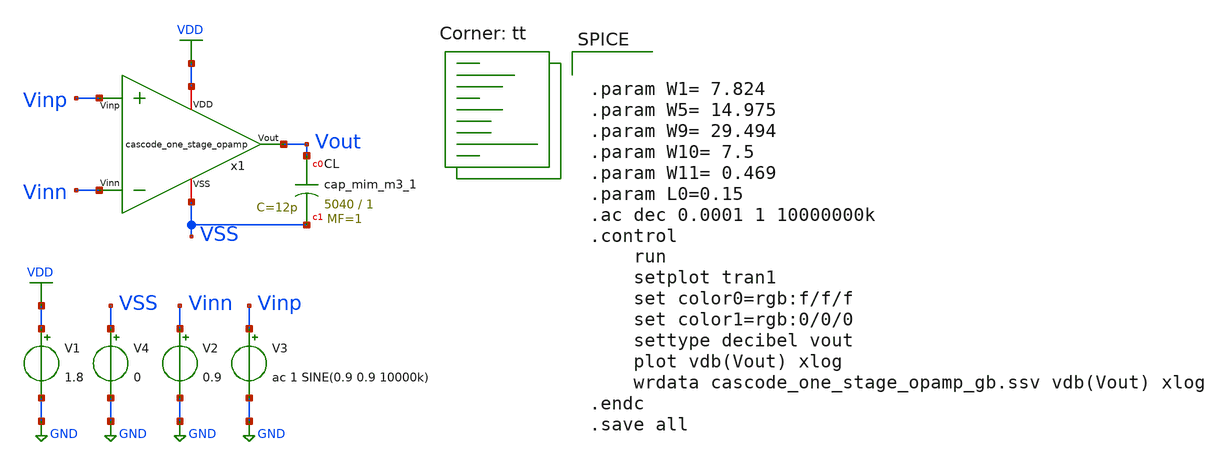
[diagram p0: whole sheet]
** sch_path: opamp_design/cascode_one_stage_opamp/cascode_one_stage_opamp_gb.sch
**.subckt cascode_one_stage_opamp_gb
V1 VDD GND 1.8
V2 Vinn GND 0.9
V3 Vinp GND ac 1 SINE(0.9 0.9 10000k)
V4 VSS GND 0
XCL Vout VSS sky130_fd_pr__cap_mim_m3_1 W=5040 L=1 MF=1 m=1
x1 VDD Vout Vinp Vinn VSS cascode_one_stage_opamp
**** begin user architecture code


.param W1= 7.824
.param W5= 14.975
.param W9= 29.494
.param W10= 7.5
.param W11= 0.469
.param L0=0.15
.ac dec 0.0001 1 10000000k
.control
	run
	setplot tran1
	set color0=rgb:f/f/f
	set color1=rgb:0/0/0
	settype decibel vout
	plot vdb(Vout) xlog
	wrdata cascode_one_stage_opamp_gb.ssv vdb(Vout) xlog
.endc
.save all


.lib $::SKYWATER_MODELS/sky130.lib.spice tt
**** end user architecture code
**.ends

* expanding   symbol:
*+  /home/ricardo/RATT_repos/Proyectos_xschem/opamp_design/cascode_one_stage_opamp/cascode_one_stage_opamp.sym # of pins=5
** sym_path: opamp_design/cascode_one_stage_opamp/cascode_one_stage_opamp.sym
** sch_path: opamp_design/cascode_one_stage_opamp/cascode_one_stage_opamp.sch
.subckt cascode_one_stage_opamp VDD Vout Vinp Vinn VSS
*.ipin Vinp
*.ipin Vinn
*.opin Vout
*.iopin VDD
*.iopin VSS
XM1 net6 Vinp net1 VSS sky130_fd_pr__nfet_01v8 L={L0} W={W1} nf=1 ad='int((nf+1)/2) * W/nf * 0.29' as='int((nf+2)/2) * W/nf * 0.29'
+ pd='2*int((nf+1)/2) * (W/nf + 0.29)' ps='2*int((nf+2)/2) * (W/nf + 0.29)' nrd='0.29 / W' nrs='0.29 / W'
+ sa=0 sb=0 sd=0 mult=1 m=1
XM2 net7 Vinn net1 VSS sky130_fd_pr__nfet_01v8 L={L0} W={W1} nf=1 ad='int((nf+1)/2) * W/nf * 0.29' as='int((nf+2)/2) * W/nf * 0.29'
+ pd='2*int((nf+1)/2) * (W/nf + 0.29)' ps='2*int((nf+2)/2) * (W/nf + 0.29)' nrd='0.29 / W' nrs='0.29 / W'
+ sa=0 sb=0 sd=0 mult=1 m=1
XM9 net1 net9 VSS VSS sky130_fd_pr__nfet_01v8 L={L0} W={W9} nf=1 ad='int((nf+1)/2) * W/nf * 0.29' as='int((nf+2)/2) * W/nf * 0.29'
+ pd='2*int((nf+1)/2) * (W/nf + 0.29)' ps='2*int((nf+2)/2) * (W/nf + 0.29)' nrd='0.29 / W' nrs='0.29 / W'
+ sa=0 sb=0 sd=0 mult=1 m=1
XM11 net2 net2 net1 VSS sky130_fd_pr__nfet_01v8 L={L0} W={W11} nf=1 ad='int((nf+1)/2) * W/nf * 0.29'
+ as='int((nf+2)/2) * W/nf * 0.29' pd='2*int((nf+1)/2) * (W/nf + 0.29)' ps='2*int((nf+2)/2) * (W/nf + 0.29)'
+ nrd='0.29 / W' nrs='0.29 / W' sa=0 sb=0 sd=0 mult=1 m=1
XM3 net3 net2 net6 VSS sky130_fd_pr__nfet_01v8 L={L0} W={W1} nf=1 ad='int((nf+1)/2) * W/nf * 0.29' as='int((nf+2)/2) * W/nf * 0.29'
+ pd='2*int((nf+1)/2) * (W/nf + 0.29)' ps='2*int((nf+2)/2) * (W/nf + 0.29)' nrd='0.29 / W' nrs='0.29 / W'
+ sa=0 sb=0 sd=0 mult=1 m=1
XM4 Vout net2 net7 VSS sky130_fd_pr__nfet_01v8 L={L0} W={W1} nf=1 ad='int((nf+1)/2) * W/nf * 0.29' as='int((nf+2)/2) * W/nf * 0.29'
+ pd='2*int((nf+1)/2) * (W/nf + 0.29)' ps='2*int((nf+2)/2) * (W/nf + 0.29)' nrd='0.29 / W' nrs='0.29 / W'
+ sa=0 sb=0 sd=0 mult=1 m=1
XM6 Vout net8 net4 VDD sky130_fd_pr__pfet_01v8 L={L0} W={W5} nf=1 ad='int((nf+1)/2) * W/nf * 0.29' as='int((nf+2)/2) * W/nf * 0.29'
+ pd='2*int((nf+1)/2) * (W/nf + 0.29)' ps='2*int((nf+2)/2) * (W/nf + 0.29)' nrd='0.29 / W' nrs='0.29 / W'
+ sa=0 sb=0 sd=0 mult=1 m=1
XM5 net3 net8 net5 VDD sky130_fd_pr__pfet_01v8 L={L0} W={W5} nf=1 ad='int((nf+1)/2) * W/nf * 0.29' as='int((nf+2)/2) * W/nf * 0.29'
+ pd='2*int((nf+1)/2) * (W/nf + 0.29)' ps='2*int((nf+2)/2) * (W/nf + 0.29)' nrd='0.29 / W' nrs='0.29 / W'
+ sa=0 sb=0 sd=0 mult=1 m=1
XM7 net5 net3 VDD VDD sky130_fd_pr__pfet_01v8 L={L0} W={W5} nf=1 ad='int((nf+1)/2) * W/nf * 0.29' as='int((nf+2)/2) * W/nf * 0.29'
+ pd='2*int((nf+1)/2) * (W/nf + 0.29)' ps='2*int((nf+2)/2) * (W/nf + 0.29)' nrd='0.29 / W' nrs='0.29 / W'
+ sa=0 sb=0 sd=0 mult=1 m=1
XM8 net4 net3 VDD VDD sky130_fd_pr__pfet_01v8 L={L0} W={W5} nf=1 ad='int((nf+1)/2) * W/nf * 0.29' as='int((nf+2)/2) * W/nf * 0.29'
+ pd='2*int((nf+1)/2) * (W/nf + 0.29)' ps='2*int((nf+2)/2) * (W/nf + 0.29)' nrd='0.29 / W' nrs='0.29 / W'
+ sa=0 sb=0 sd=0 mult=1 m=1
XM10 net2 net10 VDD VDD sky130_fd_pr__pfet_01v8 L={L0} W={W10} nf=1 ad='int((nf+1)/2) * W/nf * 0.29'
+ as='int((nf+2)/2) * W/nf * 0.29' pd='2*int((nf+1)/2) * (W/nf + 0.29)' ps='2*int((nf+2)/2) * (W/nf + 0.29)'
+ nrd='0.29 / W' nrs='0.29 / W' sa=0 sb=0 sd=0 mult=1 m=1
XM14 net9 net9 VSS VSS sky130_fd_pr__nfet_01v8 L={L0} W={W9} nf=1 ad='int((nf+1)/2) * W/nf * 0.29' as='int((nf+2)/2) * W/nf * 0.29'
+ pd='2*int((nf+1)/2) * (W/nf + 0.29)' ps='2*int((nf+2)/2) * (W/nf + 0.29)' nrd='0.29 / W' nrs='0.29 / W'
+ sa=0 sb=0 sd=0 mult=1 m=1
I0 VDD net9 100u
I1 net10 VSS 12u
XM12 net10 net10 VDD VDD sky130_fd_pr__pfet_01v8 L={L0} W={W10} nf=1 ad='int((nf+1)/2) * W/nf * 0.29'
+ as='int((nf+2)/2) * W/nf * 0.29' pd='2*int((nf+1)/2) * (W/nf + 0.29)' ps='2*int((nf+2)/2) * (W/nf + 0.29)'
+ nrd='0.29 / W' nrs='0.29 / W' sa=0 sb=0 sd=0 mult=1 m=1
I2 net8 VSS 50u
XM13 net8 net8 VDD VDD sky130_fd_pr__pfet_01v8 L={L0} W={W5} nf=1 ad='int((nf+1)/2) * W/nf * 0.29' as='int((nf+2)/2) * W/nf * 0.29'
+ pd='2*int((nf+1)/2) * (W/nf + 0.29)' ps='2*int((nf+2)/2) * (W/nf + 0.29)' nrd='0.29 / W' nrs='0.29 / W'
+ sa=0 sb=0 sd=0 mult=1 m=1
.ends

.GLOBAL VDD
.GLOBAL GND
.end
